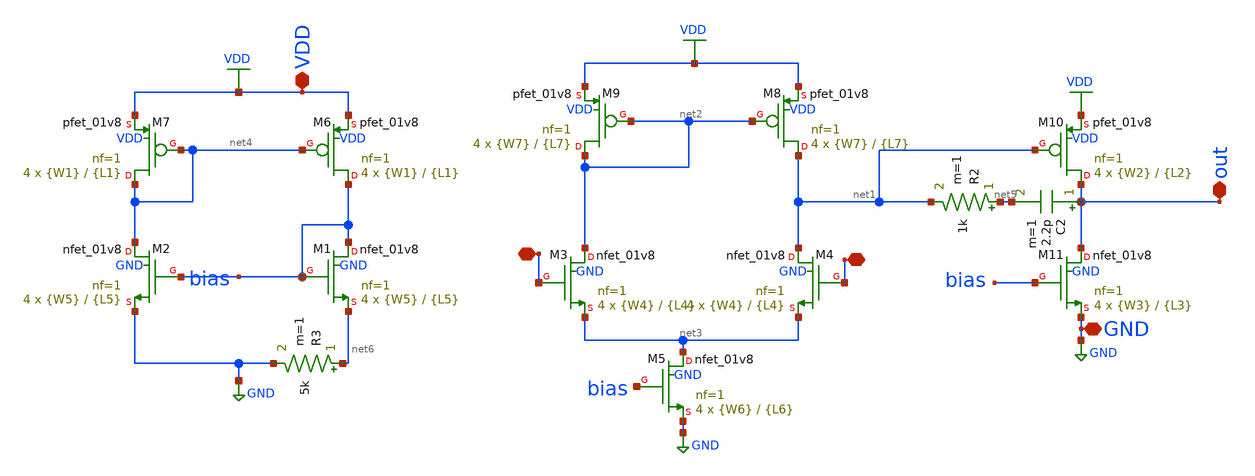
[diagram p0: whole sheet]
** sch_path: xschem/op5.sch
**.subckt op5 VDD GND - + out
*.iopin VDD
*.iopin GND
*.iopin -
*.iopin +
*.iopin out
C2 out net5 2.2p m=1
R2 net5 net1 1k m=1
XM1 bias bias net6 GND sky130_fd_pr__nfet_01v8 L={L5} W={W5} nf=1 ad='int((nf+1)/2) * W/nf * 0.29' as='int((nf+2)/2) * W/nf * 0.29'
+ pd='2*int((nf+1)/2) * (W/nf + 0.29)' ps='2*int((nf+2)/2) * (W/nf + 0.29)' nrd='0.29 / W' nrs='0.29 / W'
+ sa=0 sb=0 sd=0 mult=4 m=4
XM2 net4 bias GND GND sky130_fd_pr__nfet_01v8 L={L5} W={W5} nf=1 ad='int((nf+1)/2) * W/nf * 0.29' as='int((nf+2)/2) * W/nf * 0.29'
+ pd='2*int((nf+1)/2) * (W/nf + 0.29)' ps='2*int((nf+2)/2) * (W/nf + 0.29)' nrd='0.29 / W' nrs='0.29 / W'
+ sa=0 sb=0 sd=0 mult=4 m=4
XM3 net2 - net3 GND sky130_fd_pr__nfet_01v8 L={L4} W={W4} nf=1 ad='int((nf+1)/2) * W/nf * 0.29' as='int((nf+2)/2) * W/nf * 0.29'
+ pd='2*int((nf+1)/2) * (W/nf + 0.29)' ps='2*int((nf+2)/2) * (W/nf + 0.29)' nrd='0.29 / W' nrs='0.29 / W'
+ sa=0 sb=0 sd=0 mult=4 m=4
XM4 net1 + net3 GND sky130_fd_pr__nfet_01v8 L={L4} W={W4} nf=1 ad='int((nf+1)/2) * W/nf * 0.29' as='int((nf+2)/2) * W/nf * 0.29'
+ pd='2*int((nf+1)/2) * (W/nf + 0.29)' ps='2*int((nf+2)/2) * (W/nf + 0.29)' nrd='0.29 / W' nrs='0.29 / W'
+ sa=0 sb=0 sd=0 mult=4 m=4
XM6 bias net4 VDD VDD sky130_fd_pr__pfet_01v8 L={L1} W={W1} nf=1 ad='int((nf+1)/2) * W/nf * 0.29' as='int((nf+2)/2) * W/nf * 0.29'
+ pd='2*int((nf+1)/2) * (W/nf + 0.29)' ps='2*int((nf+2)/2) * (W/nf + 0.29)' nrd='0.29 / W' nrs='0.29 / W'
+ sa=0 sb=0 sd=0 mult=4 m=4
XM7 net4 net4 VDD VDD sky130_fd_pr__pfet_01v8 L={L1} W={W1} nf=1 ad='int((nf+1)/2) * W/nf * 0.29' as='int((nf+2)/2) * W/nf * 0.29'
+ pd='2*int((nf+1)/2) * (W/nf + 0.29)' ps='2*int((nf+2)/2) * (W/nf + 0.29)' nrd='0.29 / W' nrs='0.29 / W'
+ sa=0 sb=0 sd=0 mult=4 m=4
XM8 net1 net2 VDD VDD sky130_fd_pr__pfet_01v8 L={L7} W={W7} nf=1 ad='int((nf+1)/2) * W/nf * 0.29' as='int((nf+2)/2) * W/nf * 0.29'
+ pd='2*int((nf+1)/2) * (W/nf + 0.29)' ps='2*int((nf+2)/2) * (W/nf + 0.29)' nrd='0.29 / W' nrs='0.29 / W'
+ sa=0 sb=0 sd=0 mult=4 m=4
XM9 net2 net2 VDD VDD sky130_fd_pr__pfet_01v8 L={L7} W={W7} nf=1 ad='int((nf+1)/2) * W/nf * 0.29' as='int((nf+2)/2) * W/nf * 0.29'
+ pd='2*int((nf+1)/2) * (W/nf + 0.29)' ps='2*int((nf+2)/2) * (W/nf + 0.29)' nrd='0.29 / W' nrs='0.29 / W'
+ sa=0 sb=0 sd=0 mult=4 m=4
XM5 net3 bias GND GND sky130_fd_pr__nfet_01v8 L={L6} W={W6} nf=1 ad='int((nf+1)/2) * W/nf * 0.29' as='int((nf+2)/2) * W/nf * 0.29'
+ pd='2*int((nf+1)/2) * (W/nf + 0.29)' ps='2*int((nf+2)/2) * (W/nf + 0.29)' nrd='0.29 / W' nrs='0.29 / W'
+ sa=0 sb=0 sd=0 mult=4 m=4
XM10 out net1 VDD VDD sky130_fd_pr__pfet_01v8 L={L2} W={W2} nf=1 ad='int((nf+1)/2) * W/nf * 0.29' as='int((nf+2)/2) * W/nf * 0.29'
+ pd='2*int((nf+1)/2) * (W/nf + 0.29)' ps='2*int((nf+2)/2) * (W/nf + 0.29)' nrd='0.29 / W' nrs='0.29 / W'
+ sa=0 sb=0 sd=0 mult=4 m=4
XM11 out bias GND GND sky130_fd_pr__nfet_01v8 L={L3} W={W3} nf=1 ad='int((nf+1)/2) * W/nf * 0.29' as='int((nf+2)/2) * W/nf * 0.29'
+ pd='2*int((nf+1)/2) * (W/nf + 0.29)' ps='2*int((nf+2)/2) * (W/nf + 0.29)' nrd='0.29 / W' nrs='0.29 / W'
+ sa=0 sb=0 sd=0 mult=4 m=4
R3 net6 GND 5k m=1
**** begin user architecture code


**************
*PMOS cms
.param L1=2.7
.param W1=1.25

**************
*NMOS cms
.param L5=2
.param W5=3.5

**************
*PMOS current differential
.param L7=2.7
.param W7=1.25

**************
*differential Pair
.param L4=2.7
.param W4=1.25

**************
*NMOS current control
.param L6=2
.param W6=3.5

**************
*Second Stage
.param L2=2
.param W2=3.5

**************
*NMOS current second stage
.param L3=2
.param W3=3.5


**** end user architecture code
**.ends
.GLOBAL VDD
.GLOBAL GND
.end
